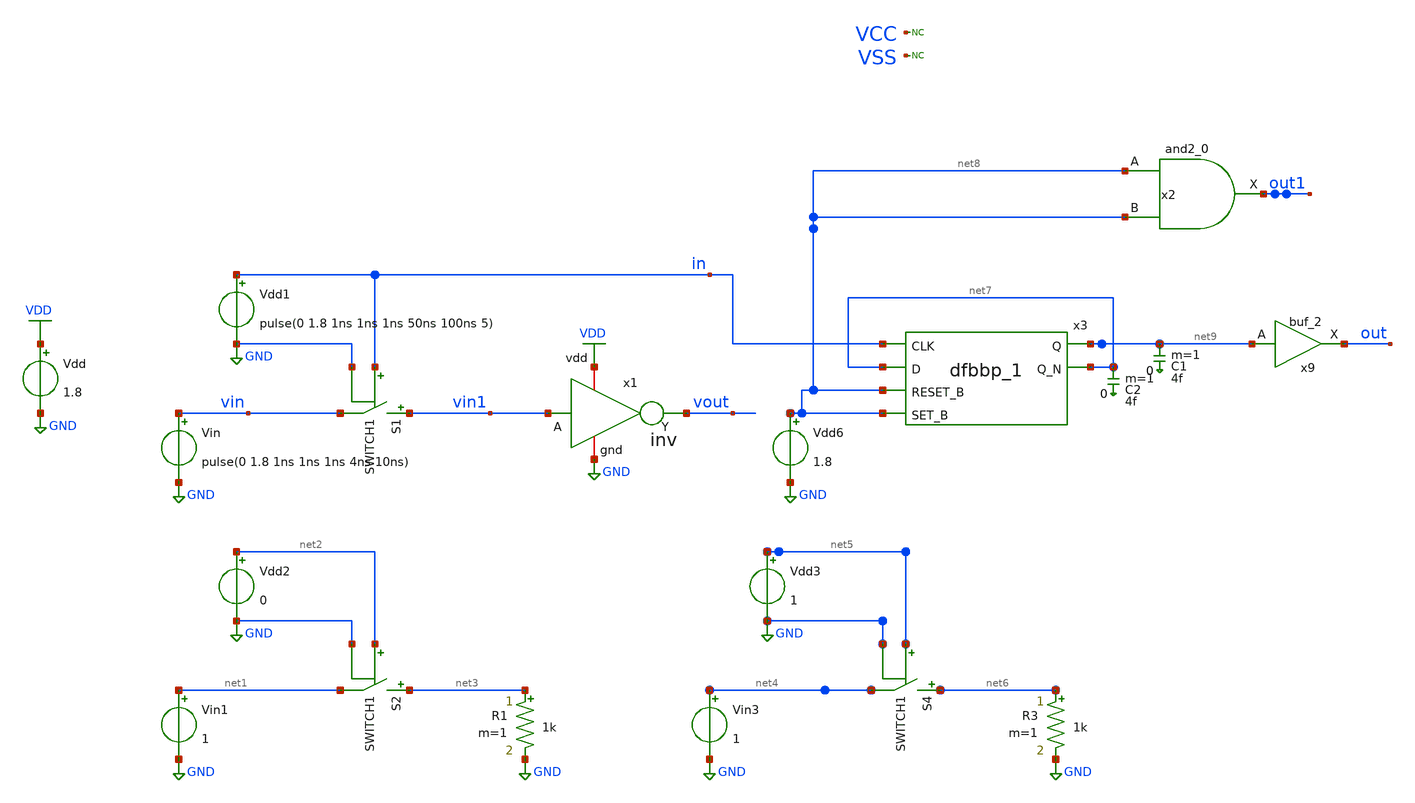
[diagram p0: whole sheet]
** sch_path: top/test/testbench/inv_tb.sch
.lib $::SKYWATER_MODELS/sky130.lib.spice tt
.include $::SKYWATER_STDCELLS/sky130_fd_sc_hd.spice

**.subckt inv_tb
x1 VDD vin1 vout GND inv
Vin vin GND pulse(0 1.8 1ns 1ns 1ns 4ns 10ns)
Vdd VDD GND 1.8
Vdd1 in GND pulse(0 1.8 1ns 1ns 1ns 50ns 100ns 5)
S1 vin1 vin in GND SWITCH1
Vin1 net1 GND 1
Vdd2 net2 GND 0
S2 net3 net1 net2 GND SWITCH1
R1 net3 GND 1k m=1
Vin3 net4 GND 1
S4 net6 net4 net5 GND SWITCH1
R3 net6 GND 1k m=1
x3 in net7 net8 net8 VSS VSS VCC VCC net9 net7 sky130_fd_sc_hd__dfbbp_1
C1 net9 0 4f m=1
Vdd3 net5 GND 1
Vdd6 net8 GND 1.8
x9 net9 VSS VSS VCC VCC out sky130_fd_sc_hd__buf_2
C2 net7 0 4f m=1
* noconn VCC
* noconn VSS
x2 net8 net8 vss vss vcc vcc out1 sky130_fd_sc_hd__and2_0
**** begin user architecture code

.model SWITCH1 sw vt=0.5 vh=0 ron=1 roff =1G




.tran 0.01n 500n
.save all
.control
.param vcc = 1.8
vvcc vcc 0 dc vcc
vvss vss 0 0

pre_set auto_bridge_d_out =  ( ".model auto_dac dac_bridge(out_low = 0 out_high = 1.8 out_undef=0.9
+ t_rise=0.2e-9 t_fall=0.2e-9)"  "auto_bridge%d [ %s ] [ %s ] auto_dac" )

pre_set auto_bridge_d_in =  ( ".model auto_adc adc_bridge(in_low = 0.6 in_high = 1.2
+ rise_delay=0.2e-9 fall_delay=0.2e-9)"  "auto_bridge%d [ %s ] [ %s ] auto_adc" )

run

plot in out+2 out1+4 vcc+6

.endc


**** end user architecture code
**.ends

* expanding   symbol:  /foss/designs/test/design/inv/inv.sym # of pins=4
** sym_path: top/test/design/inv/inv.sym
** sch_path: top/test/design/inv/inv.sch
.subckt inv vdd A Y gnd
*.ipin A
*.opin Y
*.iopin vdd
*.iopin gnd
XM11 Y A vdd vdd sky130_fd_pr__pfet_01v8 L=0.15 W=1 nf=1 ad='int((nf+1)/2) * W/nf * 0.29' as='int((nf+2)/2) * W/nf * 0.29'
+ pd='2*int((nf+1)/2) * (W/nf + 0.29)' ps='2*int((nf+2)/2) * (W/nf + 0.29)' nrd='0.29 / W' nrs='0.29 / W'
+ sa=0 sb=0 sd=0 mult=1 m=1
XM2 Y A gnd gnd sky130_fd_pr__nfet_01v8 L=0.15 W=1 nf=1 ad='int((1 + 1)/2) * 1 / 1 * 0.29' as='int((1 + 2)/2) * 1 / 1 * 0.29'
+ pd='2*int((1 + 1)/2) * (1 / 1 + 0.29)' ps='2*int((1 + 2)/2) * (1 / 1 + 0.29)' nrd='0.29 / 1 ' nrs='0.29 / 1 '
+ sa=0 sb=0 sd=0 mult=1 m=1
.ends

.GLOBAL VDD
.GLOBAL GND
.end
